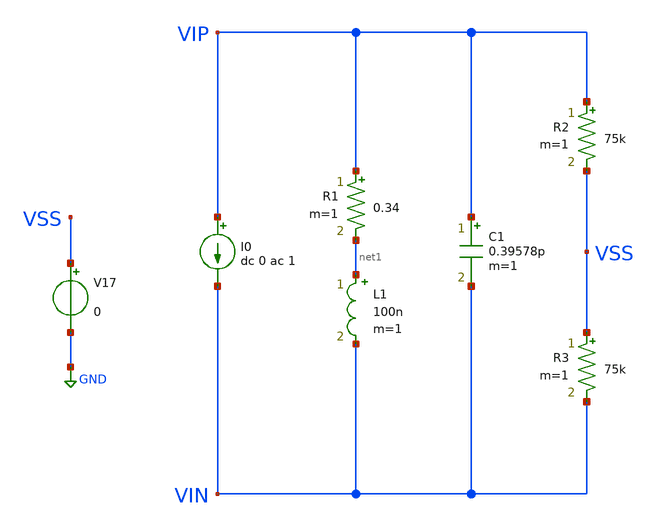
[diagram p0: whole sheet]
** sch_path: analog/tb/tb_coil.sch
**.subckt tb_coil
L1 net1 VIN 100n m=1
R1 VIP net1 0.34 m=1
C1 VIP VIN 0.39578p m=1
V17 VSS GND 0
R2 VIP VSS 75k m=1
R3 VSS VIN 75k m=1
I0 VIP VIN dc 0 ac 1
**** begin user architecture code



.save all
.save V(VIP) V(VIN) V(VIP, VIN)
.save I(VPORT)


.control
  set filetype=ascii        ; ASCII .raw (human-readable)
    run
    ac dec 1000 1Meg 1000Meg
    *tran 0.1u 100u
    let ZIN  = v(VIP, VIN)
    let ABSZ = abs(ZIN)
    let IMZ  = imag(ZIN)
    let REZ  = real(ZIN)
    let Q    = IMZ/REZ
    meas ac F_res when IMZ=0
    write tb_coil1.raw ABSZ Q
    set appendwrite
.endc



.lib cornerMOSlv.lib mos_tt

**** end user architecture code
**.ends
.GLOBAL GND
.end
